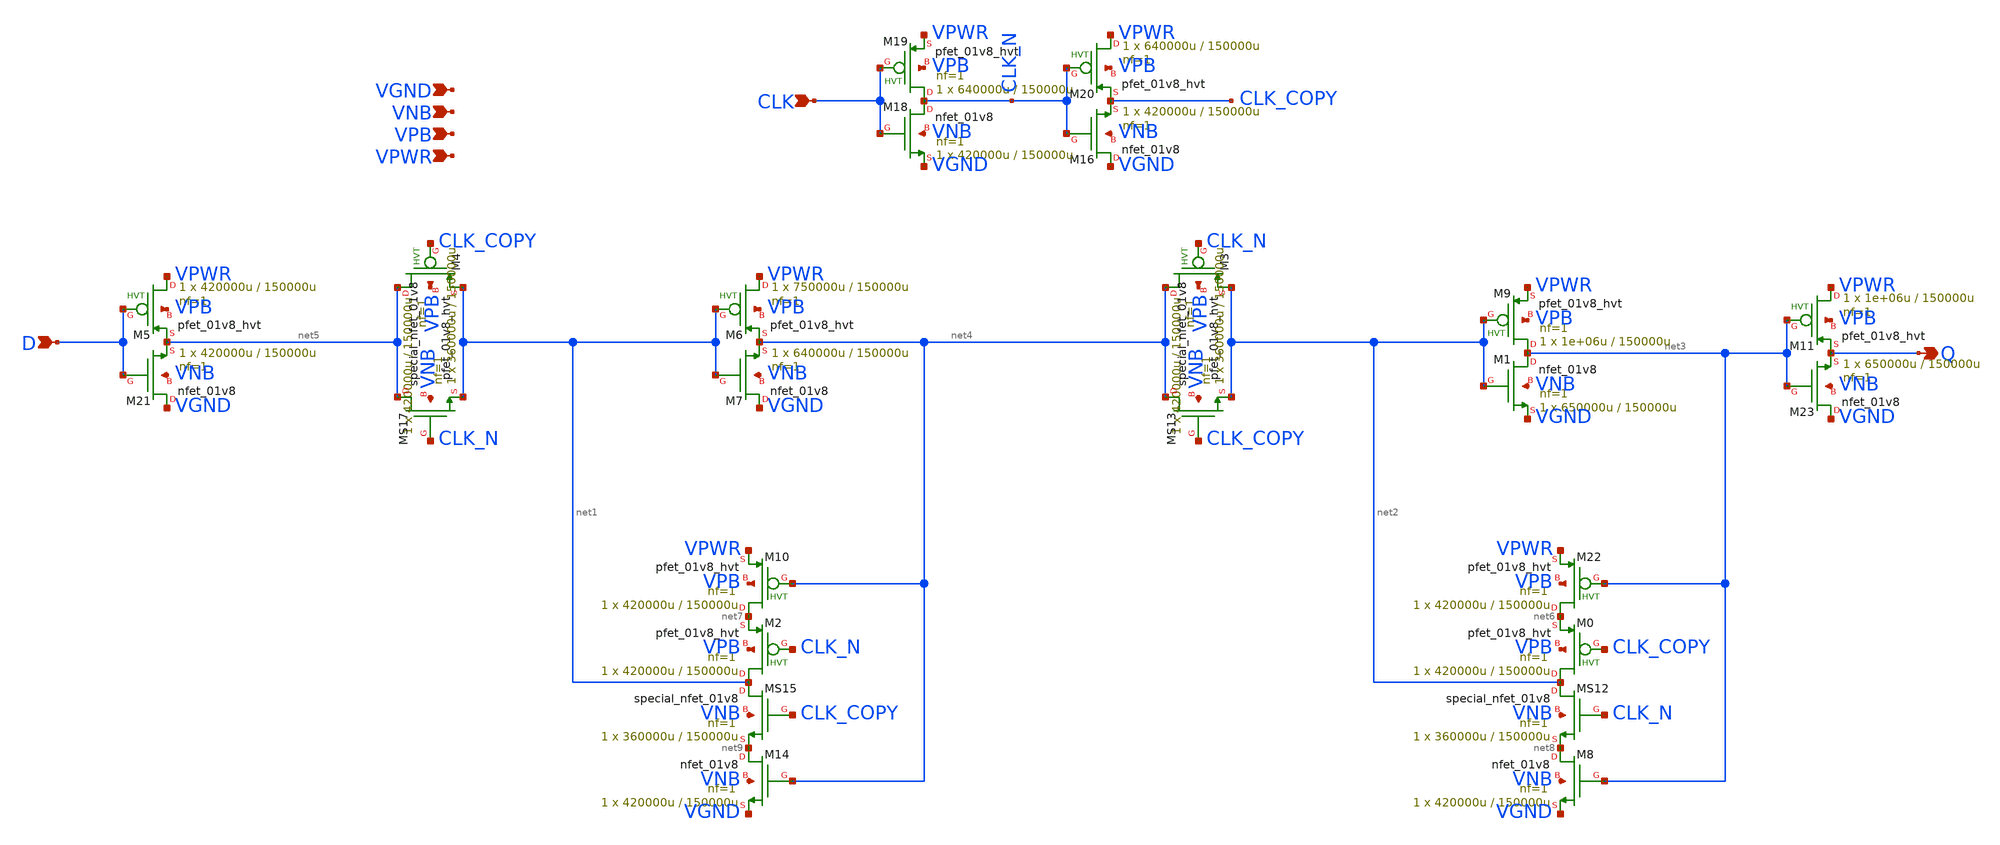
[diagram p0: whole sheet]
** sch_path: schematics/dfxtp/sky130_fd_sc_hd__dfxtp_1.sch
**.subckt sky130_fd_sc_hd__dfxtp_1 CLK Q D VGND VNB VPB VPWR
*.ipin CLK
*.opin Q
*.ipin D
*.ipin VGND
*.ipin VNB
*.ipin VPB
*.ipin VPWR
XM0 net2 CLK_COPY net6 VPB sky130_fd_pr__pfet_01v8_hvt L=150000u W=420000u nf=1 ad='int((1 + 1)/2) * 420000u / 1 * 0.29'
+ as='int((1 + 2)/2) * 420000u / 1 * 0.29' pd='2*int((1 + 1)/2) * (420000u / 1 + 0.29)' ps='2*int((1 + 2)/2) * (420000u / 1 + 0.29)'
+ nrd='0.29 / 420000u ' nrs='0.29 / 420000u ' sa=0 sb=0 sd=0 mult=1 m=1
XM1 net3 net2 VGND VNB sky130_fd_pr__nfet_01v8 L=150000u W=650000u nf=1 ad='int((1 + 1)/2) * 650000u / 1 * 0.29'
+ as='int((1 + 2)/2) * 650000u / 1 * 0.29' pd='2*int((1 + 1)/2) * (650000u / 1 + 0.29)' ps='2*int((1 + 2)/2) * (650000u / 1 + 0.29)'
+ nrd='0.29 / 650000u ' nrs='0.29 / 650000u ' sa=0 sb=0 sd=0 mult=1 m=1
XM2 net1 CLK_N net7 VPB sky130_fd_pr__pfet_01v8_hvt L=150000u W=420000u nf=1 ad='int((1 + 1)/2) * 420000u / 1 * 0.29'
+ as='int((1 + 2)/2) * 420000u / 1 * 0.29' pd='2*int((1 + 1)/2) * (420000u / 1 + 0.29)' ps='2*int((1 + 2)/2) * (420000u / 1 + 0.29)'
+ nrd='0.29 / 420000u ' nrs='0.29 / 420000u ' sa=0 sb=0 sd=0 mult=1 m=1
XM3 net4 CLK_N net2 VPB sky130_fd_pr__pfet_01v8_hvt L=150000u W=420000u nf=1 ad='int((1 + 1)/2) * 420000u / 1 * 0.29'
+ as='int((1 + 2)/2) * 420000u / 1 * 0.29' pd='2*int((1 + 1)/2) * (420000u / 1 + 0.29)' ps='2*int((1 + 2)/2) * (420000u / 1 + 0.29)'
+ nrd='0.29 / 420000u ' nrs='0.29 / 420000u ' sa=0 sb=0 sd=0 mult=1 m=1
XM4 net5 CLK_COPY net1 VPB sky130_fd_pr__pfet_01v8_hvt L=150000u W=420000u nf=1 ad='int((1 + 1)/2) * 420000u / 1 * 0.29'
+ as='int((1 + 2)/2) * 420000u / 1 * 0.29' pd='2*int((1 + 1)/2) * (420000u / 1 + 0.29)' ps='2*int((1 + 2)/2) * (420000u / 1 + 0.29)'
+ nrd='0.29 / 420000u ' nrs='0.29 / 420000u ' sa=0 sb=0 sd=0 mult=1 m=1
XM5 VPWR D net5 VPB sky130_fd_pr__pfet_01v8_hvt L=150000u W=420000u nf=1 ad='int((1 + 1)/2) * 420000u / 1 * 0.29'
+ as='int((1 + 2)/2) * 420000u / 1 * 0.29' pd='2*int((1 + 1)/2) * (420000u / 1 + 0.29)' ps='2*int((1 + 2)/2) * (420000u / 1 + 0.29)'
+ nrd='0.29 / 420000u ' nrs='0.29 / 420000u ' sa=0 sb=0 sd=0 mult=1 m=1
XM6 VPWR net1 net4 VPB sky130_fd_pr__pfet_01v8_hvt L=150000u W=750000u nf=1 ad='int((1 + 1)/2) * 750000u / 1 * 0.29'
+ as='int((1 + 2)/2) * 750000u / 1 * 0.29' pd='2*int((1 + 1)/2) * (750000u / 1 + 0.29)' ps='2*int((1 + 2)/2) * (750000u / 1 + 0.29)'
+ nrd='0.29 / 750000u ' nrs='0.29 / 750000u ' sa=0 sb=0 sd=0 mult=1 m=1
XM7 VGND net1 net4 VNB sky130_fd_pr__nfet_01v8 L=150000u W=640000u nf=1 ad='int((1 + 1)/2) * 640000u / 1 * 0.29'
+ as='int((1 + 2)/2) * 640000u / 1 * 0.29' pd='2*int((1 + 1)/2) * (640000u / 1 + 0.29)' ps='2*int((1 + 2)/2) * (640000u / 1 + 0.29)'
+ nrd='0.29 / 640000u ' nrs='0.29 / 640000u ' sa=0 sb=0 sd=0 mult=1 m=1
XM8 net8 net3 VGND VNB sky130_fd_pr__nfet_01v8 L=150000u W=420000u nf=1 ad='int((1 + 1)/2) * 420000u / 1 * 0.29'
+ as='int((1 + 2)/2) * 420000u / 1 * 0.29' pd='2*int((1 + 1)/2) * (420000u / 1 + 0.29)' ps='2*int((1 + 2)/2) * (420000u / 1 + 0.29)'
+ nrd='0.29 / 420000u ' nrs='0.29 / 420000u ' sa=0 sb=0 sd=0 mult=1 m=1
XM9 net3 net2 VPWR VPB sky130_fd_pr__pfet_01v8_hvt L=150000u W=1e+06u nf=1 ad='int((1 + 1)/2) * 1e+06u / 1 * 0.29'
+ as='int((1 + 2)/2) * 1e+06u / 1 * 0.29' pd='2*int((1 + 1)/2) * (1e+06u / 1 + 0.29)' ps='2*int((1 + 2)/2) * (1e+06u / 1 + 0.29)'
+ nrd='0.29 / 1e+06u ' nrs='0.29 / 1e+06u ' sa=0 sb=0 sd=0 mult=1 m=1
XM10 net7 net4 VPWR VPB sky130_fd_pr__pfet_01v8_hvt L=150000u W=420000u nf=1 ad='int((1 + 1)/2) * 420000u / 1 * 0.29'
+ as='int((1 + 2)/2) * 420000u / 1 * 0.29' pd='2*int((1 + 1)/2) * (420000u / 1 + 0.29)' ps='2*int((1 + 2)/2) * (420000u / 1 + 0.29)'
+ nrd='0.29 / 420000u ' nrs='0.29 / 420000u ' sa=0 sb=0 sd=0 mult=1 m=1
XM11 VPWR net3 Q VPB sky130_fd_pr__pfet_01v8_hvt L=150000u W=1e+06u nf=1 ad='int((1 + 1)/2) * 1e+06u / 1 * 0.29'
+ as='int((1 + 2)/2) * 1e+06u / 1 * 0.29' pd='2*int((1 + 1)/2) * (1e+06u / 1 + 0.29)' ps='2*int((1 + 2)/2) * (1e+06u / 1 + 0.29)'
+ nrd='0.29 / 1e+06u ' nrs='0.29 / 1e+06u ' sa=0 sb=0 sd=0 mult=1 m=1
XMS12 net2 CLK_N net8 VNB sky130_fd_pr__special_nfet_01v8 L=150000u W=360000u nf=1 ad='int((1 + 1)/2) * 360000u / 1 * 0.29'
+ as='int((1 + 2)/2) * 360000u / 1 * 0.29' pd='2*int((1 + 1)/2) * (360000u / 1 + 0.29)' ps='2*int((1 + 2)/2) * (360000u / 1 + 0.29)'
+ nrd='0.29 / 360000u ' nrs='0.29 / 360000u ' sa=0 sb=0 sd=0 mult=1 m=1
XMS13 net4 CLK_COPY net2 VNB sky130_fd_pr__special_nfet_01v8 L=150000u W=360000u nf=1 ad='int((1 + 1)/2) * 360000u / 1 * 0.29'
+ as='int((1 + 2)/2) * 360000u / 1 * 0.29' pd='2*int((1 + 1)/2) * (360000u / 1 + 0.29)' ps='2*int((1 + 2)/2) * (360000u / 1 + 0.29)'
+ nrd='0.29 / 360000u ' nrs='0.29 / 360000u ' sa=0 sb=0 sd=0 mult=1 m=1
XM14 net9 net4 VGND VNB sky130_fd_pr__nfet_01v8 L=150000u W=420000u nf=1 ad='int((1 + 1)/2) * 420000u / 1 * 0.29'
+ as='int((1 + 2)/2) * 420000u / 1 * 0.29' pd='2*int((1 + 1)/2) * (420000u / 1 + 0.29)' ps='2*int((1 + 2)/2) * (420000u / 1 + 0.29)'
+ nrd='0.29 / 420000u ' nrs='0.29 / 420000u ' sa=0 sb=0 sd=0 mult=1 m=1
XMS15 net1 CLK_COPY net9 VNB sky130_fd_pr__special_nfet_01v8 L=150000u W=360000u nf=1 ad='int((1 + 1)/2) * 360000u / 1 * 0.29'
+ as='int((1 + 2)/2) * 360000u / 1 * 0.29' pd='2*int((1 + 1)/2) * (360000u / 1 + 0.29)' ps='2*int((1 + 2)/2) * (360000u / 1 + 0.29)'
+ nrd='0.29 / 360000u ' nrs='0.29 / 360000u ' sa=0 sb=0 sd=0 mult=1 m=1
XM16 VGND CLK_N CLK_COPY VNB sky130_fd_pr__nfet_01v8 L=150000u W=420000u nf=1 ad='int((1 + 1)/2) * 420000u / 1 * 0.29'
+ as='int((1 + 2)/2) * 420000u / 1 * 0.29' pd='2*int((1 + 1)/2) * (420000u / 1 + 0.29)' ps='2*int((1 + 2)/2) * (420000u / 1 + 0.29)'
+ nrd='0.29 / 420000u ' nrs='0.29 / 420000u ' sa=0 sb=0 sd=0 mult=1 m=1
XMS17 net5 CLK_N net1 VNB sky130_fd_pr__special_nfet_01v8 L=150000u W=360000u nf=1 ad='int((1 + 1)/2) * 360000u / 1 * 0.29'
+ as='int((1 + 2)/2) * 360000u / 1 * 0.29' pd='2*int((1 + 1)/2) * (360000u / 1 + 0.29)' ps='2*int((1 + 2)/2) * (360000u / 1 + 0.29)'
+ nrd='0.29 / 360000u ' nrs='0.29 / 360000u ' sa=0 sb=0 sd=0 mult=1 m=1
XM18 CLK_N CLK VGND VNB sky130_fd_pr__nfet_01v8 L=150000u W=420000u nf=1 ad='int((1 + 1)/2) * 420000u / 1 * 0.29'
+ as='int((1 + 2)/2) * 420000u / 1 * 0.29' pd='2*int((1 + 1)/2) * (420000u / 1 + 0.29)' ps='2*int((1 + 2)/2) * (420000u / 1 + 0.29)'
+ nrd='0.29 / 420000u ' nrs='0.29 / 420000u ' sa=0 sb=0 sd=0 mult=1 m=1
XM19 CLK_N CLK VPWR VPB sky130_fd_pr__pfet_01v8_hvt L=150000u W=640000u nf=1 ad='int((1 + 1)/2) * 640000u / 1 * 0.29'
+ as='int((1 + 2)/2) * 640000u / 1 * 0.29' pd='2*int((1 + 1)/2) * (640000u / 1 + 0.29)' ps='2*int((1 + 2)/2) * (640000u / 1 + 0.29)'
+ nrd='0.29 / 640000u ' nrs='0.29 / 640000u ' sa=0 sb=0 sd=0 mult=1 m=1
XM20 VPWR CLK_N CLK_COPY VPB sky130_fd_pr__pfet_01v8_hvt L=150000u W=640000u nf=1 ad='int((1 + 1)/2) * 640000u / 1 * 0.29'
+ as='int((1 + 2)/2) * 640000u / 1 * 0.29' pd='2*int((1 + 1)/2) * (640000u / 1 + 0.29)' ps='2*int((1 + 2)/2) * (640000u / 1 + 0.29)'
+ nrd='0.29 / 640000u ' nrs='0.29 / 640000u ' sa=0 sb=0 sd=0 mult=1 m=1
XM21 VGND D net5 VNB sky130_fd_pr__nfet_01v8 L=150000u W=420000u nf=1 ad='int((1 + 1)/2) * 420000u / 1 * 0.29'
+ as='int((1 + 2)/2) * 420000u / 1 * 0.29' pd='2*int((1 + 1)/2) * (420000u / 1 + 0.29)' ps='2*int((1 + 2)/2) * (420000u / 1 + 0.29)'
+ nrd='0.29 / 420000u ' nrs='0.29 / 420000u ' sa=0 sb=0 sd=0 mult=1 m=1
XM22 net6 net3 VPWR VPB sky130_fd_pr__pfet_01v8_hvt L=150000u W=420000u nf=1 ad='int((1 + 1)/2) * 420000u / 1 * 0.29'
+ as='int((1 + 2)/2) * 420000u / 1 * 0.29' pd='2*int((1 + 1)/2) * (420000u / 1 + 0.29)' ps='2*int((1 + 2)/2) * (420000u / 1 + 0.29)'
+ nrd='0.29 / 420000u ' nrs='0.29 / 420000u ' sa=0 sb=0 sd=0 mult=1 m=1
XM23 VGND net3 Q VNB sky130_fd_pr__nfet_01v8 L=150000u W=650000u nf=1 ad='int((1 + 1)/2) * 650000u / 1 * 0.29'
+ as='int((1 + 2)/2) * 650000u / 1 * 0.29' pd='2*int((1 + 1)/2) * (650000u / 1 + 0.29)' ps='2*int((1 + 2)/2) * (650000u / 1 + 0.29)'
+ nrd='0.29 / 650000u ' nrs='0.29 / 650000u ' sa=0 sb=0 sd=0 mult=1 m=1
**.ends
.end
